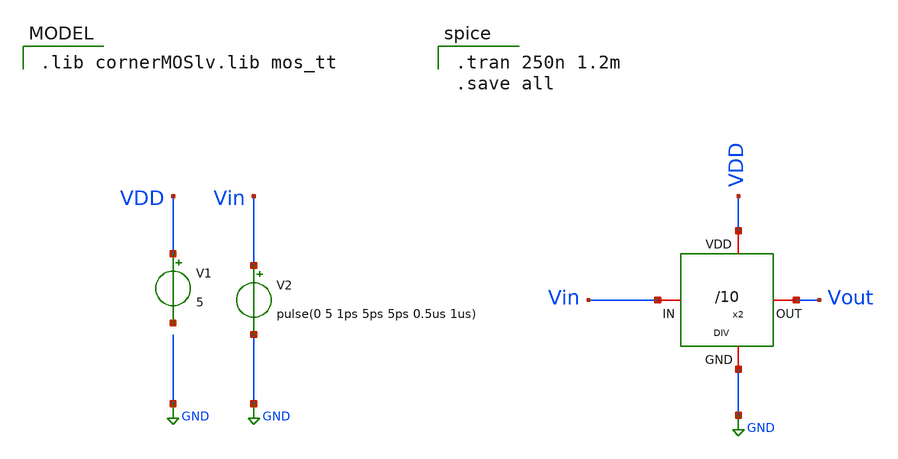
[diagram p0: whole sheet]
** sch_path: unic_cass_wrapper_user_project/ROs_reliability/DIV_TB.sch
**.subckt DIV_TB
V1 VDD net1 5
V2 Vin GND pulse(0 5 1ps 5ps 5ps 0.5us 1us)
x2 VDD Vout Vin GND DIV
**** begin user architecture code

.tran 250n 1.2m
.save all

 .lib cornerMOSlv.lib mos_tt

**** end user architecture code
**.ends
.GLOBAL GND
.end
